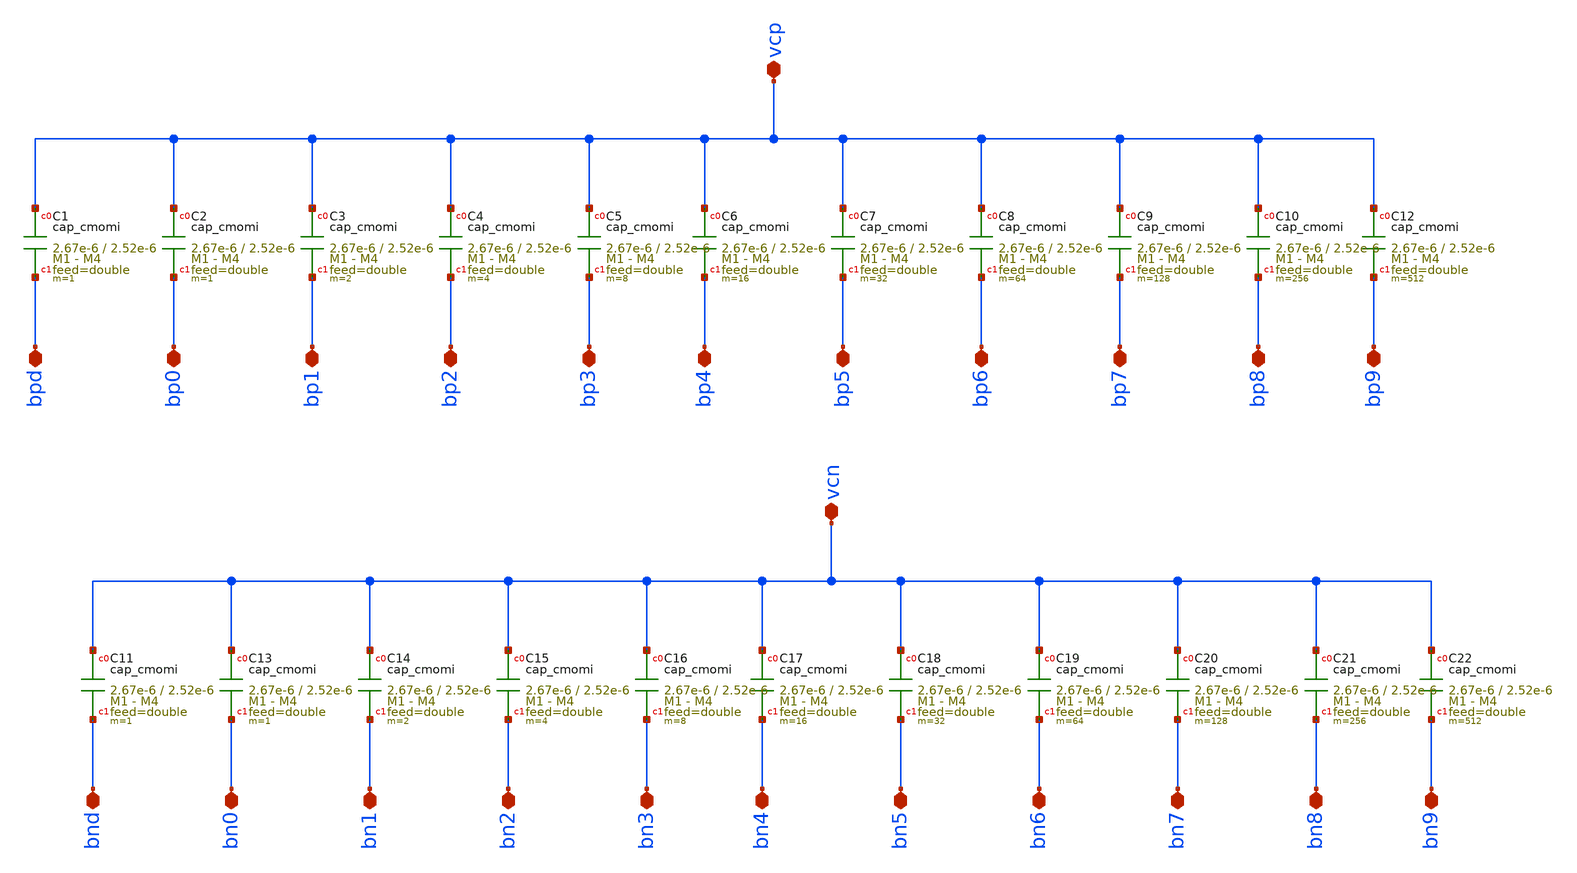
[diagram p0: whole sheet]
** sch_path: circuit_files/sar_adc_test/xschem/cdac_caps_10b_diff.sch
**.subckt cdac_caps_10b_diff vcp vcn bpd bp0 bp1 bp2 bp3 bp4 bp5 bp6 bp7 bp8 bp9 bnd bn1 bn2 bn3 bn4
*+ bn5 bn6 bn7 bn8 bn9 bn0
*.iopin vcp
*.iopin vcn
*.iopin bpd
*.iopin bp0
*.iopin bp1
*.iopin bp2
*.iopin bp3
*.iopin bp4
*.iopin bp5
*.iopin bp6
*.iopin bp7
*.iopin bp8
*.iopin bp9
*.iopin bnd
*.iopin bn1
*.iopin bn2
*.iopin bn3
*.iopin bn4
*.iopin bn5
*.iopin bn6
*.iopin bn7
*.iopin bn8
*.iopin bn9
*.iopin bn0
XC1 vcp bpd cap_cmomi w=2.67e-6 l=2.52e-6 mmin=1 mmax=4 feed=double subblock=0 m=1 mm_ok=1
XC2 vcp bp0 cap_cmomi w=2.67e-6 l=2.52e-6 mmin=1 mmax=4 feed=double subblock=0 m=1 mm_ok=1
XC3 vcp bp1 cap_cmomi w=2.67e-6 l=2.52e-6 mmin=1 mmax=4 feed=double subblock=0 m=2 mm_ok=1
XC4 vcp bp2 cap_cmomi w=2.67e-6 l=2.52e-6 mmin=1 mmax=4 feed=double subblock=0 m=4 mm_ok=1
XC5 vcp bp3 cap_cmomi w=2.67e-6 l=2.52e-6 mmin=1 mmax=4 feed=double subblock=0 m=8 mm_ok=1
XC6 vcp bp4 cap_cmomi w=2.67e-6 l=2.52e-6 mmin=1 mmax=4 feed=double subblock=0 m=16 mm_ok=1
XC7 vcp bp5 cap_cmomi w=2.67e-6 l=2.52e-6 mmin=1 mmax=4 feed=double subblock=0 m=32 mm_ok=1
XC8 vcp bp6 cap_cmomi w=2.67e-6 l=2.52e-6 mmin=1 mmax=4 feed=double subblock=0 m=64 mm_ok=1
XC9 vcp bp7 cap_cmomi w=2.67e-6 l=2.52e-6 mmin=1 mmax=4 feed=double subblock=0 m=128 mm_ok=1
XC10 vcp bp8 cap_cmomi w=2.67e-6 l=2.52e-6 mmin=1 mmax=4 feed=double subblock=0 m=256 mm_ok=1
XC12 vcp bp9 cap_cmomi w=2.67e-6 l=2.52e-6 mmin=1 mmax=4 feed=double subblock=0 m=512 mm_ok=1
XC11 vcn bnd cap_cmomi w=2.67e-6 l=2.52e-6 mmin=1 mmax=4 feed=double subblock=0 m=1 mm_ok=1
XC13 vcn bn0 cap_cmomi w=2.67e-6 l=2.52e-6 mmin=1 mmax=4 feed=double subblock=0 m=1 mm_ok=1
XC14 vcn bn1 cap_cmomi w=2.67e-6 l=2.52e-6 mmin=1 mmax=4 feed=double subblock=0 m=2 mm_ok=1
XC15 vcn bn2 cap_cmomi w=2.67e-6 l=2.52e-6 mmin=1 mmax=4 feed=double subblock=0 m=4 mm_ok=1
XC16 vcn bn3 cap_cmomi w=2.67e-6 l=2.52e-6 mmin=1 mmax=4 feed=double subblock=0 m=8 mm_ok=1
XC17 vcn bn4 cap_cmomi w=2.67e-6 l=2.52e-6 mmin=1 mmax=4 feed=double subblock=0 m=16 mm_ok=1
XC18 vcn bn5 cap_cmomi w=2.67e-6 l=2.52e-6 mmin=1 mmax=4 feed=double subblock=0 m=32 mm_ok=1
XC19 vcn bn6 cap_cmomi w=2.67e-6 l=2.52e-6 mmin=1 mmax=4 feed=double subblock=0 m=64 mm_ok=1
XC20 vcn bn7 cap_cmomi w=2.67e-6 l=2.52e-6 mmin=1 mmax=4 feed=double subblock=0 m=128 mm_ok=1
XC21 vcn bn8 cap_cmomi w=2.67e-6 l=2.52e-6 mmin=1 mmax=4 feed=double subblock=0 m=256 mm_ok=1
XC22 vcn bn9 cap_cmomi w=2.67e-6 l=2.52e-6 mmin=1 mmax=4 feed=double subblock=0 m=512 mm_ok=1
**.ends
.end
